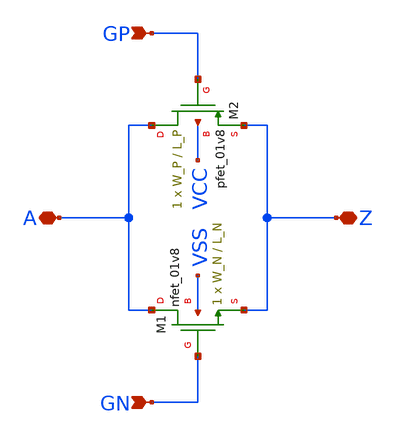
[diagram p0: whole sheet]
** sch_path: sky130_tests/passgate.sch
* Copyright 2020 Stefan Frederik Schippers
* Licensed under the Apache License, Version 2.0 (the "License");
* you may not use this file except in compliance with the License.
* You may obtain a copy of the License at
* https://www.apache.org/licenses/LICENSE-2.0
* Unless required by applicable law or agreed to in writing, software
* distributed under the License is distributed on an "AS IS" BASIS,
* WITHOUT WARRANTIES OR CONDITIONS OF ANY KIND, either express or implied.
* See the License for the specific language governing permissions and
* limitations under the License.
**.subckt passgate A Z GP GN
*.iopin A
*.iopin Z
*.ipin GP
*.ipin GN
XM1 A GN Z VSS sky130_fd_pr__nfet_01v8 W=W_N L=L_N ad='w * 0.29u' pd='w + 2 * 0.29u' as='w * 0.29u' ps='w + 2 * 0.29u'
+ nrd=0 nrs=0 sa=0 sb=0 sd=0 nf=1 mult=1
XM2 A GP Z VCC sky130_fd_pr__pfet_01v8 W=W_P L=L_P ad='w * 0.29u' pd='w + 2 * 0.29u' as='w * 0.29u' ps='w + 2 * 0.29u'
+ nrd=0 nrs=0 sa=0 sb=0 sd=0 nf=1 mult=1
**.ends
.end
